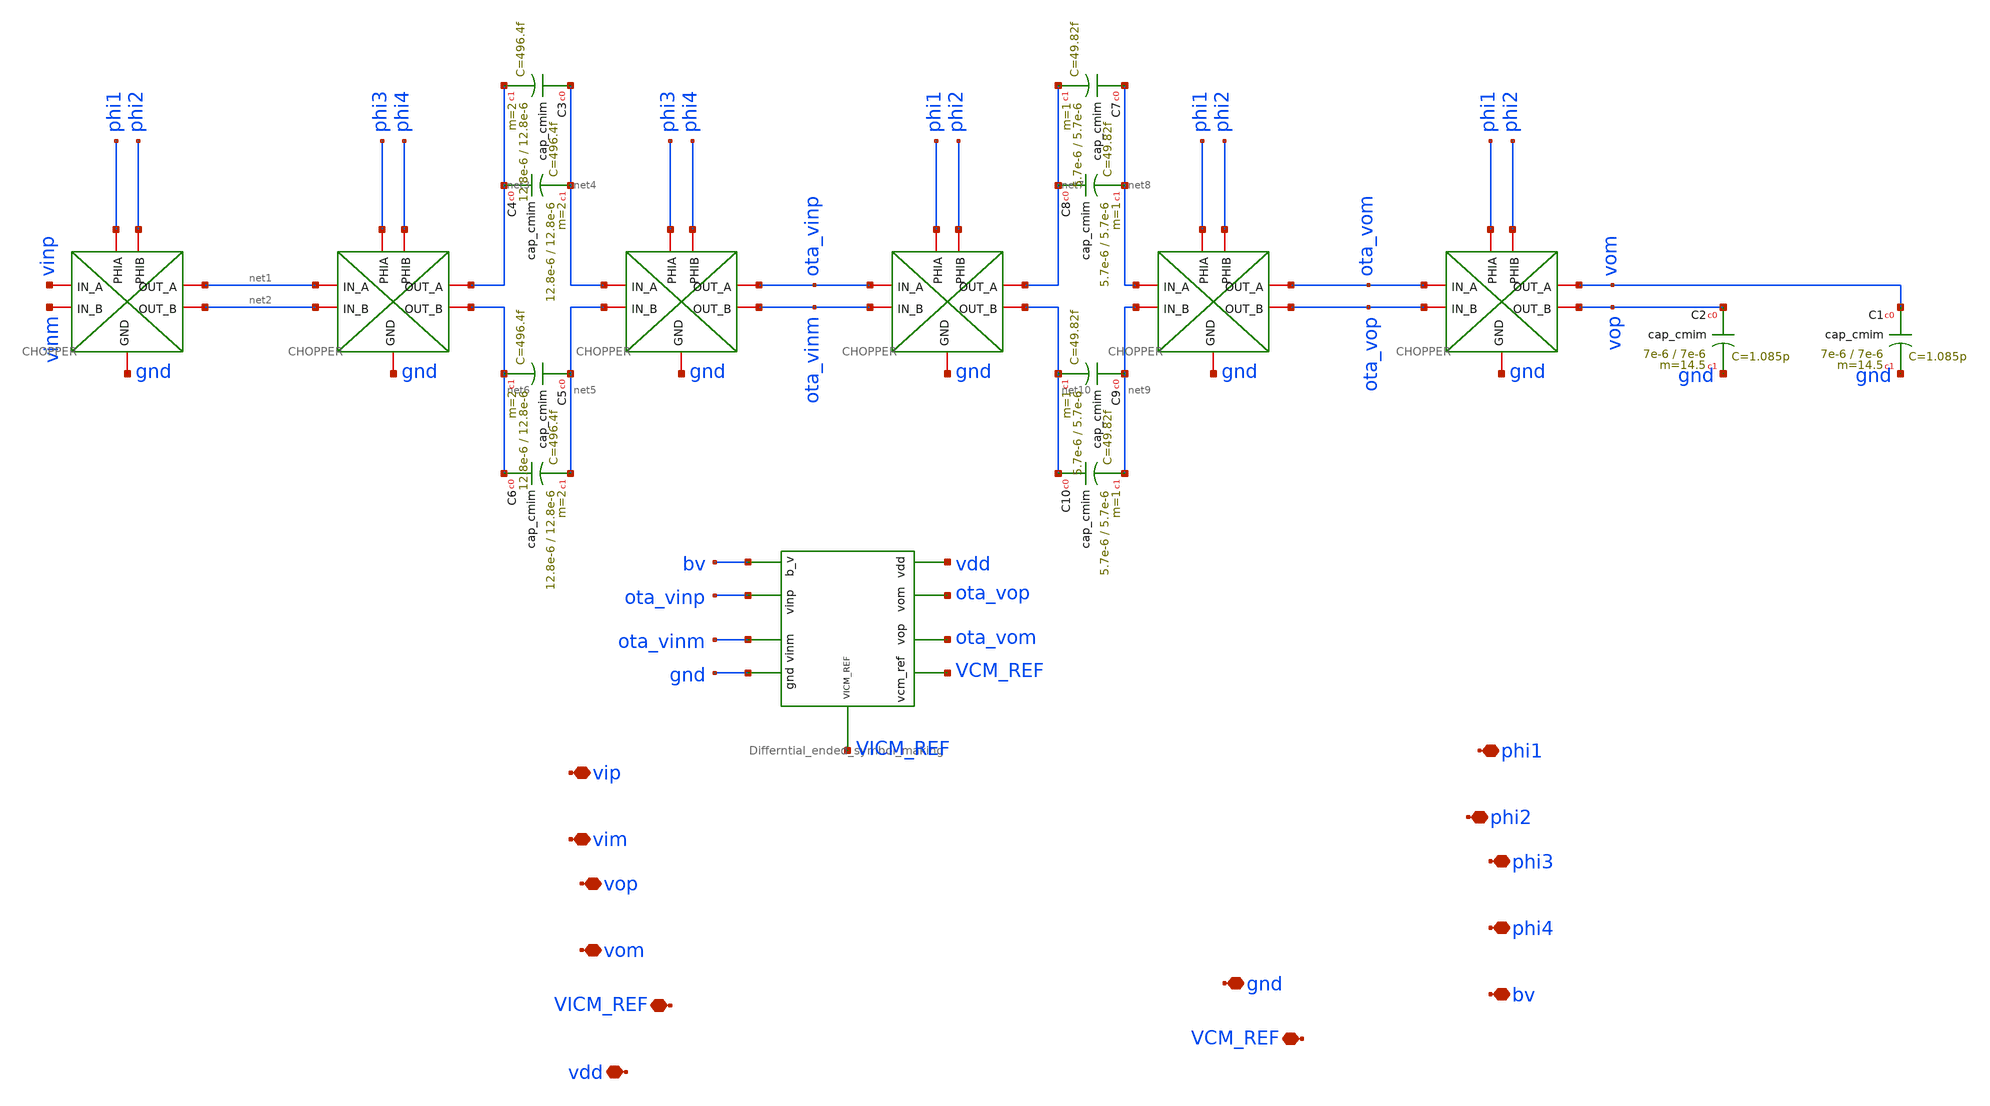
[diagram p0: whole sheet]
** sch_path: imp_boost_tech.sch
**.subckt imp_boost_tech vip vim vop vom phi1 phi2 phi3 phi4 VICM_REF bv gnd vdd VCM_REF
*.iopin vip
*.iopin vim
*.iopin vop
*.iopin vom
*.iopin phi1
*.iopin phi2
*.iopin phi3
*.iopin phi4
*.iopin VICM_REF
*.iopin bv
*.iopin gnd
*.iopin vdd
*.iopin VCM_REF
x3 phi3 net3 net1 phi4 net6 net2 gnd CHOPPER
x4 phi3 ota_vinp net4 phi4 ota_vinm net5 gnd CHOPPER
x5 phi1 net7 ota_vinp phi2 net10 ota_vinm gnd CHOPPER
x6 phi1 ota_vom net8 phi2 ota_vop net9 gnd CHOPPER
x7 phi1 vom ota_vom phi2 vop ota_vop gnd CHOPPER
XC3 net4 net3 cap_cmim w=12.8e-6 l=12.8e-6 m=2 mm_ok=1
XC4 net3 net4 cap_cmim w=12.8e-6 l=12.8e-6 m=2 mm_ok=1
XC5 net5 net6 cap_cmim w=12.8e-6 l=12.8e-6 m=2 mm_ok=1
XC6 net6 net5 cap_cmim w=12.8e-6 l=12.8e-6 m=2 mm_ok=1
XC7 net8 net7 cap_cmim w=5.7e-6 l=5.7e-6 m=1 mm_ok=1
XC8 net7 net8 cap_cmim w=5.7e-6 l=5.7e-6 m=1 mm_ok=1
XC9 net9 net10 cap_cmim w=5.7e-6 l=5.7e-6 m=1 mm_ok=1
XC10 net10 net9 cap_cmim w=5.7e-6 l=5.7e-6 m=1 mm_ok=1
x2 vdd VCM_REF ota_vop ota_vom gnd bv ota_vinm ota_vinp VICM_REF Differntial_ended_symbol_making
XC1 vom gnd cap_cmim w=7e-6 l=7e-6 m=14.5 mm_ok=1
XC2 vop gnd cap_cmim w=7e-6 l=7e-6 m=14.5 mm_ok=1
x1 phi1 net1 vinp phi2 net2 vinm gnd CHOPPER
**.ends

* expanding   symbol:
*+  /home/prabhas/unic-cass-example/UNI-CASS_Project/final_Design_file/CHOPPER.sym # of pins=7
** sym_path: /home/prabhas/unic-cass-example/UNI-CASS_Project/final_Design_file/CHOPPER.sym
** sch_path: /home/prabhas/unic-cass-example/UNI-CASS_Project/final_Design_file/CHOPPER.sch
.subckt CHOPPER PHIA OUT_A IN_A PHIB OUT_B IN_B GND
*.iopin IN_A
*.iopin IN_B
*.iopin OUT_B
*.iopin OUT_A
*.iopin PHIA
*.iopin PHIB
*.iopin GND
XM1 OUT_A PHIA IN_A GND sg13_hv_nmos w=0.3u l=0.45u ng=1 m=1 mm_ok=1
XM2 OUT_B PHIA IN_B GND sg13_hv_nmos w=0.3u l=0.45u ng=1 m=1 mm_ok=1
XM3 OUT_B PHIB IN_A GND sg13_hv_nmos w=0.3u l=0.45u ng=1 m=1 mm_ok=1
XM4 IN_B PHIB OUT_A GND sg13_hv_nmos w=0.3u l=0.45u ng=1 m=1 mm_ok=1
.ends


* expanding   symbol:
*+  /home/prabhas/unic-cass-example/UNI-CASS_Project/final_Design_file/Differntial_ended_symbol_making.sym # of pins=9
** sym_path: Differntial_ended_symbol_making.sym
** sch_path: Differntial_ended_symbol_making.sch
.subckt Differntial_ended_symbol_making vdd vcm_ref vom vop gnd b_v vinm vinp VICM_REF
*.iopin b_v
*.iopin vdd
*.iopin vinm
*.iopin vcm_ref
*.iopin vinp
*.iopin vop
*.iopin vom
*.iopin gnd
*.iopin VICM_REF
XM7 vop nbias gnd gnd sg13_hv_nmos w=4u l=2u ng=1 m=1 mm_ok=1
XM8 vop vinm tail tail sg13_hv_pmos w=9u l=1u ng=1 m=1 mm_ok=1
XM9 vom nbias gnd gnd sg13_hv_nmos w=4u l=2u ng=1 m=1 mm_ok=1
XM10 vom vinp tail tail sg13_hv_pmos w=9u l=1u ng=1 m=1 mm_ok=1
XM11 tail b_v vdd vdd sg13_hv_pmos w=4u l=1u ng=1 m=4 mm_ok=1
XM6 net1 net1 gnd gnd sg13_hv_nmos w=1u l=0.5u ng=1 m=1 mm_ok=1
XM13 net1 vop tail_cmfb tail_cmfb sg13_hv_pmos w=2.25u l=0.50u ng=1 m=1 mm_ok=1
XM14 nbias net1 gnd gnd sg13_hv_nmos w=1u l=0.5u ng=1 m=1 mm_ok=1
XM15 nbias vcm_ref tail_cmfb tail_cmfb sg13_hv_pmos w=0.5u l=4.5u ng=1 m=1 mm_ok=1
XM16 tail_cmfb b_v vdd vdd sg13_hv_pmos w=4u l=1u ng=1 m=4 mm_ok=1
XM17 net1 vom tail_cmfb tail_cmfb sg13_hv_pmos w=2.25u l=0.50u ng=1 m=1 mm_ok=1
C5 nbias gnd 1p m=1
XM1 b_v b_v vdd vdd sg13_hv_pmos w=4u l=1u ng=1 m=1 mm_ok=1
XM2 VICM_REF vinm vinm vinm sg13_hv_pmos w=10u l=1u ng=1 m=1 mm_ok=1
XM3 VICM_REF vinp vinp vinp sg13_hv_pmos w=10u l=1u ng=1 m=1 mm_ok=1
.ends

.end
